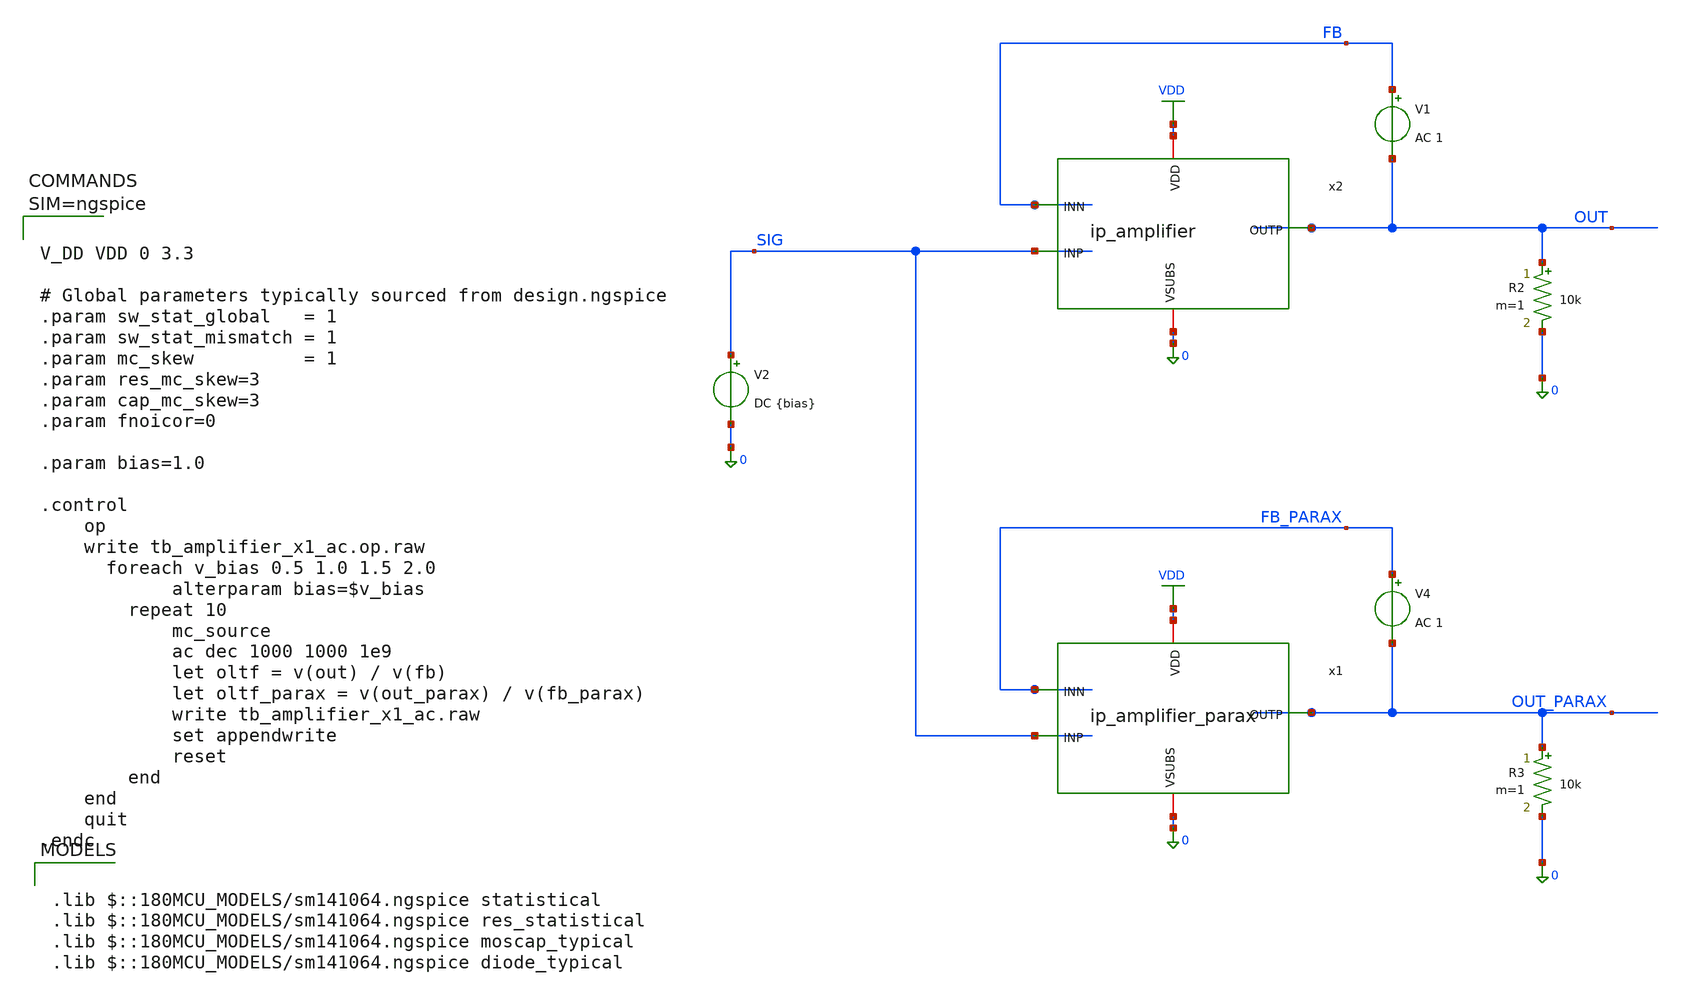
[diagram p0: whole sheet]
** sch_path: xschem/tb_amplifier_x1_ac.sch
**.subckt tb_amplifier_x1_ac
V2 SIG 0 DC {bias}
x2 VDD OUT SIG FB 0 ip_amplifier
R2 OUT 0 10k m=1
V1 FB OUT AC 1
x1 VDD OUT_PARAX SIG FB_PARAX 0 ip_amplifier_parax
R3 OUT_PARAX 0 10k m=1
V4 FB_PARAX OUT_PARAX AC 1
**** begin user architecture code

.lib $::180MCU_MODELS/sm141064.ngspice statistical
.lib $::180MCU_MODELS/sm141064.ngspice res_statistical
.lib $::180MCU_MODELS/sm141064.ngspice moscap_typical
.lib $::180MCU_MODELS/sm141064.ngspice diode_typical




V_DD VDD 0 3.3

# Global parameters typically sourced from design.ngspice
.param sw_stat_global   = 1
.param sw_stat_mismatch = 1
.param mc_skew          = 1
.param res_mc_skew=3
.param cap_mc_skew=3
.param fnoicor=0

.param bias=1.0

.control
	op
	write tb_amplifier_x1_ac.op.raw
  	foreach v_bias 0.5 1.0 1.5 2.0
    		alterparam bias=$v_bias
		repeat 10
			mc_source
			ac dec 1000 1000 1e9
			let oltf = v(out) / v(fb)
			let oltf_parax = v(out_parax) / v(fb_parax)
			write tb_amplifier_x1_ac.raw
			set appendwrite
			reset
		end
	end
	quit
.endc



**** end user architecture code
**.ends

* expanding   symbol:  ip_amplifier.sym # of pins=5
** sym_path: xschem/ip_amplifier.sym
** sch_path: xschem/ip_amplifier.sch
.subckt ip_amplifier VDD OUTP INP INN VSUBS
*.iopin VDD
*.iopin VSUBS
*.ipin INP
*.ipin INN
*.opin OUTP
XM1 net10 INP net8 VDD pfet_06v0 L=0.7u W=11.0u nf=1 ad='int((nf+1)/2) * W/nf * 0.18u' as='int((nf+2)/2) * W/nf * 0.18u'
+ pd='2*int((nf+1)/2) * (W/nf + 0.18u)' ps='2*int((nf+2)/2) * (W/nf + 0.18u)' nrd='0.18u / W' nrs='0.18u / W'
+ sa=0 sb=0 sd=0 m=2 par=2
XM2 net9 INN net8 VDD pfet_06v0 L=0.7u W=11.0u nf=1 ad='int((nf+1)/2) * W/nf * 0.18u' as='int((nf+2)/2) * W/nf * 0.18u'
+ pd='2*int((nf+1)/2) * (W/nf + 0.18u)' ps='2*int((nf+2)/2) * (W/nf + 0.18u)' nrd='0.18u / W' nrs='0.18u / W'
+ sa=0 sb=0 sd=0 m=2 par=2
XM5 net10 net1 VSUBS vsubs nfet_06v0 L=2u W=5u nf=1 ad='int((nf+1)/2) * W/nf * 0.18u' as='int((nf+2)/2) * W/nf * 0.18u'
+ pd='2*int((nf+1)/2) * (W/nf + 0.18u)' ps='2*int((nf+2)/2) * (W/nf + 0.18u)' nrd='0.18u / W' nrs='0.18u / W'
+ sa=0 sb=0 sd=0 m=1 par=1
XM6 net9 net1 VSUBS vsubs nfet_06v0 L=2u W=5u nf=1 ad='int((nf+1)/2) * W/nf * 0.18u' as='int((nf+2)/2) * W/nf * 0.18u'
+ pd='2*int((nf+1)/2) * (W/nf + 0.18u)' ps='2*int((nf+2)/2) * (W/nf + 0.18u)' nrd='0.18u / W' nrs='0.18u / W'
+ sa=0 sb=0 sd=0 m=1 par=1
XM3 net3 net1 VSUBS vsubs nfet_06v0 L=1u W=12.5u nf=1 ad='int((nf+1)/2) * W/nf * 0.18u' as='int((nf+2)/2) * W/nf * 0.18u'
+ pd='2*int((nf+1)/2) * (W/nf + 0.18u)' ps='2*int((nf+2)/2) * (W/nf + 0.18u)' nrd='0.18u / W' nrs='0.18u / W'
+ sa=0 sb=0 sd=0 m=2 par=2
XM4 net2 net1 VSUBS vsubs nfet_06v0 L=1u W=5u nf=1 ad='int((nf+1)/2) * W/nf * 0.18u' as='int((nf+2)/2) * W/nf * 0.18u'
+ pd='2*int((nf+1)/2) * (W/nf + 0.18u)' ps='2*int((nf+2)/2) * (W/nf + 0.18u)' nrd='0.18u / W' nrs='0.18u / W'
+ sa=0 sb=0 sd=0 m=1 par=1
XM7 net1 net1 net3 vsubs nfet_06v0 L=0.7u W=14u nf=1 ad='int((nf+1)/2) * W/nf * 0.18u' as='int((nf+2)/2) * W/nf * 0.18u'
+ pd='2*int((nf+1)/2) * (W/nf + 0.18u)' ps='2*int((nf+2)/2) * (W/nf + 0.18u)' nrd='0.18u / W' nrs='0.18u / W'
+ sa=0 sb=0 sd=0 m=2 par=2
XM8 net4 net1 net2 vsubs nfet_06v0 L=0.7u W=14u nf=1 ad='int((nf+1)/2) * W/nf * 0.18u' as='int((nf+2)/2) * W/nf * 0.18u'
+ pd='2*int((nf+1)/2) * (W/nf + 0.18u)' ps='2*int((nf+2)/2) * (W/nf + 0.18u)' nrd='0.18u / W' nrs='0.18u / W'
+ sa=0 sb=0 sd=0 m=2 par=2
XM9 net5 net7 VDD VDD pfet_06v0 L=1u W=6u nf=1 ad='int((nf+1)/2) * W/nf * 0.18u' as='int((nf+2)/2) * W/nf * 0.18u'
+ pd='2*int((nf+1)/2) * (W/nf + 0.18u)' ps='2*int((nf+2)/2) * (W/nf + 0.18u)' nrd='0.18u / W' nrs='0.18u / W'
+ sa=0 sb=0 sd=0 m=1 par=1
XM10 net6 net7 VDD VDD pfet_06v0 L=1u W=6u nf=1 ad='int((nf+1)/2) * W/nf * 0.18u' as='int((nf+2)/2) * W/nf * 0.18u'
+ pd='2*int((nf+1)/2) * (W/nf + 0.18u)' ps='2*int((nf+2)/2) * (W/nf + 0.18u)' nrd='0.18u / W' nrs='0.18u / W'
+ sa=0 sb=0 sd=0 m=1 par=1
XM11 net7 net7 net5 VDD pfet_06v0 L=0.7u W=14u nf=1 ad='int((nf+1)/2) * W/nf * 0.18u' as='int((nf+2)/2) * W/nf * 0.18u'
+ pd='2*int((nf+1)/2) * (W/nf + 0.18u)' ps='2*int((nf+2)/2) * (W/nf + 0.18u)' nrd='0.18u / W' nrs='0.18u / W'
+ sa=0 sb=0 sd=0 m=2 par=2
XM12 net8 net7 net6 VDD pfet_06v0 L=0.7u W=14u nf=1 ad='int((nf+1)/2) * W/nf * 0.18u' as='int((nf+2)/2) * W/nf * 0.18u'
+ pd='2*int((nf+1)/2) * (W/nf + 0.18u)' ps='2*int((nf+2)/2) * (W/nf + 0.18u)' nrd='0.18u / W' nrs='0.18u / W'
+ sa=0 sb=0 sd=0 m=2 par=2
XM13 net11 net1 net9 vsubs nfet_06v0 L=0.7u W=12u nf=1 ad='int((nf+1)/2) * W/nf * 0.18u' as='int((nf+2)/2) * W/nf * 0.18u'
+ pd='2*int((nf+1)/2) * (W/nf + 0.18u)' ps='2*int((nf+2)/2) * (W/nf + 0.18u)' nrd='0.18u / W' nrs='0.18u / W'
+ sa=0 sb=0 sd=0 m=1 par=1
XM14 COMP net1 net10 vsubs nfet_06v0 L=0.7u W=12u nf=1 ad='int((nf+1)/2) * W/nf * 0.18u' as='int((nf+2)/2) * W/nf * 0.18u'
+ pd='2*int((nf+1)/2) * (W/nf + 0.18u)' ps='2*int((nf+2)/2) * (W/nf + 0.18u)' nrd='0.18u / W' nrs='0.18u / W'
+ sa=0 sb=0 sd=0 m=1 par=1
XM15 net11 net11 VDD VDD pfet_06v0 L=0.7u W=12u nf=1 ad='int((nf+1)/2) * W/nf * 0.18u' as='int((nf+2)/2) * W/nf * 0.18u'
+ pd='2*int((nf+1)/2) * (W/nf + 0.18u)' ps='2*int((nf+2)/2) * (W/nf + 0.18u)' nrd='0.18u / W' nrs='0.18u / W'
+ sa=0 sb=0 sd=0 m=1 par=1
XM16 COMP net11 VDD VDD pfet_06v0 L=0.7u W=12u nf=1 ad='int((nf+1)/2) * W/nf * 0.18u' as='int((nf+2)/2) * W/nf * 0.18u'
+ pd='2*int((nf+1)/2) * (W/nf + 0.18u)' ps='2*int((nf+2)/2) * (W/nf + 0.18u)' nrd='0.18u / W' nrs='0.18u / W'
+ sa=0 sb=0 sd=0 m=1 par=1
XM17 OUTP COMP VDD VDD pfet_06v0 L=0.7u W=12u nf=1 ad='int((nf+1)/2) * W/nf * 0.18u' as='int((nf+2)/2) * W/nf * 0.18u'
+ pd='2*int((nf+1)/2) * (W/nf + 0.18u)' ps='2*int((nf+2)/2) * (W/nf + 0.18u)' nrd='0.18u / W' nrs='0.18u / W'
+ sa=0 sb=0 sd=0 m=5 par=5
XM18 OUTP net10 VSUBS vsubs nfet_06v0 L=0.7u W=12u nf=1 ad='int((nf+1)/2) * W/nf * 0.18u' as='int((nf+2)/2) * W/nf * 0.18u'
+ pd='2*int((nf+1)/2) * (W/nf + 0.18u)' ps='2*int((nf+2)/2) * (W/nf + 0.18u)' nrd='0.18u / W' nrs='0.18u / W'
+ sa=0 sb=0 sd=0 m=3 par=3
XR3 net1 net14 vsubs ppolyf_u_1k_6p0 r_width=1e-6 r_length=6e-6 m=1
XR6 net14 net13 vsubs ppolyf_u_1k_6p0 r_width=1e-6 r_length=6e-6 m=1
XR7 net13 net12 vsubs ppolyf_u_1k_6p0 r_width=1e-6 r_length=6e-6 m=1
XR8 net12 net15 vsubs ppolyf_u_1k_6p0 r_width=1e-6 r_length=4e-6 m=1
Vmeas VDD net15 0
Vmeas1 net7 net4 0
XC1 OUTP net16 cap_nmos_03v3 c_width=12e-6 c_length=18e-6 m=1
XC2 COMP net17 cap_nmos_03v3 c_width=12e-6 c_length=18e-6 m=1
XR12 net16 COMP vsubs ppolyf_u_1k_6p0 r_width=1e-6 r_length=10e-6 m=1
XR16 OUTP net17 vsubs ppolyf_u_1k_6p0 r_width=1e-6 r_length=10e-6 m=1
.ends


* expanding   symbol:  ip_amplifier_parax.sym # of pins=5
** sym_path: xschem/ip_amplifier.sym
.include [file normalize ./parax/ip_amplifier.sim.spice]
.GLOBAL VDD
.end
